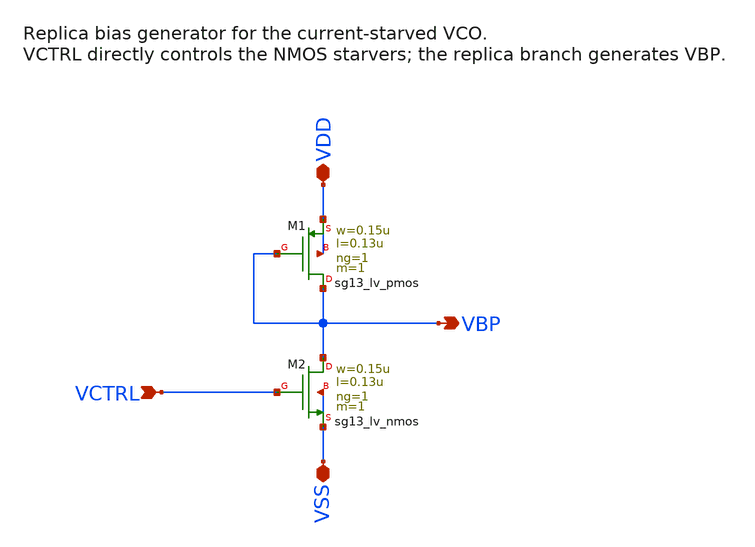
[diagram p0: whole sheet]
** sch_path: macros/pll_analog/schematic/xschem/vco_bias.sch
**.subckt vco_bias VCTRL VBP VDD VSS
*.ipin VCTRL
*.opin VBP
*.iopin VDD
*.iopin VSS
XM1 VBP VBP VDD VDD sg13_lv_pmos w=0.15u l=0.13u ng=1 m=1 mm_ok=1
XM2 VBP VCTRL VSS VSS sg13_lv_nmos w=0.15u l=0.13u ng=1 m=1 mm_ok=1
**.ends
.end
